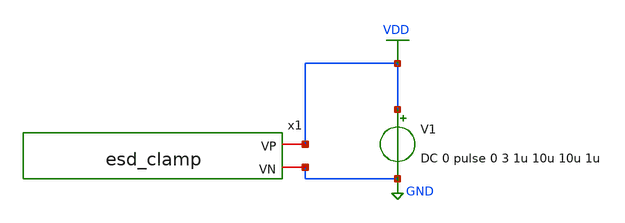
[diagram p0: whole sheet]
** sch_path: xschem/test/test_esd.sch
**.subckt test_esd
x1 VDD GND esd_clamp
V1 VDD GND DC 0 pulse 0 3 1u 10u 10u 1u
**** begin user architecture code


*.options savecurrents
.option warn=1
.control
set wr_vecnames
set wr_singlescale
set hcopydevtype=svg
set ITL1=10000

let min_temp=0
let var_temp = min_temp
let max_temp=100
let temp_step=100

option temp=0


tran 100n 30u

plot i(v1)
plot v(vdd) v(x1.vgm1) v(x1.vgm5)


.endc




* .include ../../tia.spice
* .include ../../filter_diff.spice
* .include ../../cmm_sense3.spice

.include esd_clamp.spice



* .lib $::SKYWATER_MODELS/sky130.lib.spice hl
.lib $::SKYWATER_MODELS/sky130.lib.spice.tt.red tt
* .lib /home/simon/share/pdk/sky130A/libs.tech/ngspice/sky130.lib.spice.tt.red tt

**** end user architecture code
**.ends

* expanding   symbol:  /home/simon/code/asic/analog/esd/esd_clamp.sym # of pins=2
** sym_path: xschem/esd/esd_clamp.sym
** sch_path: xschem/esd/esd_clamp.sch
.subckt esd_clamp VP VN
*.iopin VP
*.iopin VN
XD1 net1 VGM1 sky130_fd_pr__diode_pw2nd_05v5 area=10e12 pj=4e6
XM3 VGM5 VN VP VP sky130_fd_pr__pfet_01v8 L=1 W=2 nf=1 ad='int((nf+1)/2) * W/nf * 0.29' as='int((nf+2)/2) * W/nf * 0.29'
+ pd='2*int((nf+1)/2) * (W/nf + 0.29)' ps='2*int((nf+2)/2) * (W/nf + 0.29)' nrd='0.29 / W' nrs='0.29 / W'
+ sa=0 sb=0 sd=0 mult=1 m=1
XM4 VGM1 VGM5 VP VP sky130_fd_pr__pfet_01v8 L=0.3 W=2 nf=1 ad='int((nf+1)/2) * W/nf * 0.29' as='int((nf+2)/2) * W/nf * 0.29'
+ pd='2*int((nf+1)/2) * (W/nf + 0.29)' ps='2*int((nf+2)/2) * (W/nf + 0.29)' nrd='0.29 / W' nrs='0.29 / W'
+ sa=0 sb=0 sd=0 mult=10 m=10
XM5 VGM1 VGM5 VN VN sky130_fd_pr__nfet_01v8_lvt L=1 W=2 nf=1 ad='int((nf+1)/2) * W/nf * 0.29' as='int((nf+2)/2) * W/nf * 0.29'
+ pd='2*int((nf+1)/2) * (W/nf + 0.29)' ps='2*int((nf+2)/2) * (W/nf + 0.29)' nrd='0.29 / W' nrs='0.29 / W'
+ sa=0 sb=0 sd=0 mult=1 m=1
XD2 VP net1 sky130_fd_pr__diode_pw2nd_05v5 area=10e12 pj=4e6
XM1 VP VGM1 VN VN sky130_fd_pr__nfet_01v8 L=0.3 W=2 nf=1 ad='int((nf+1)/2) * W/nf * 0.29' as='int((nf+2)/2) * W/nf * 0.29'
+ pd='2*int((nf+1)/2) * (W/nf + 0.29)' ps='2*int((nf+2)/2) * (W/nf + 0.29)' nrd='0.29 / W' nrs='0.29 / W'
+ sa=0 sb=0 sd=0 mult=1000 m=1000
XM6 net1 VP VN VN sky130_fd_pr__nfet_01v8 L=1 W=1 nf=1 ad='int((nf+1)/2) * W/nf * 0.29' as='int((nf+2)/2) * W/nf * 0.29'
+ pd='2*int((nf+1)/2) * (W/nf + 0.29)' ps='2*int((nf+2)/2) * (W/nf + 0.29)' nrd='0.29 / W' nrs='0.29 / W'
+ sa=0 sb=0 sd=0 mult=1 m=1
XM2 VGM5 VGM1 VN VN sky130_fd_pr__nfet_01v8 L=0.3 W=2 nf=1 ad='int((nf+1)/2) * W/nf * 0.29' as='int((nf+2)/2) * W/nf * 0.29'
+ pd='2*int((nf+1)/2) * (W/nf + 0.29)' ps='2*int((nf+2)/2) * (W/nf + 0.29)' nrd='0.29 / W' nrs='0.29 / W'
+ sa=0 sb=0 sd=0 mult=10 m=10
.ends

.GLOBAL VDD
.GLOBAL GND
.end
